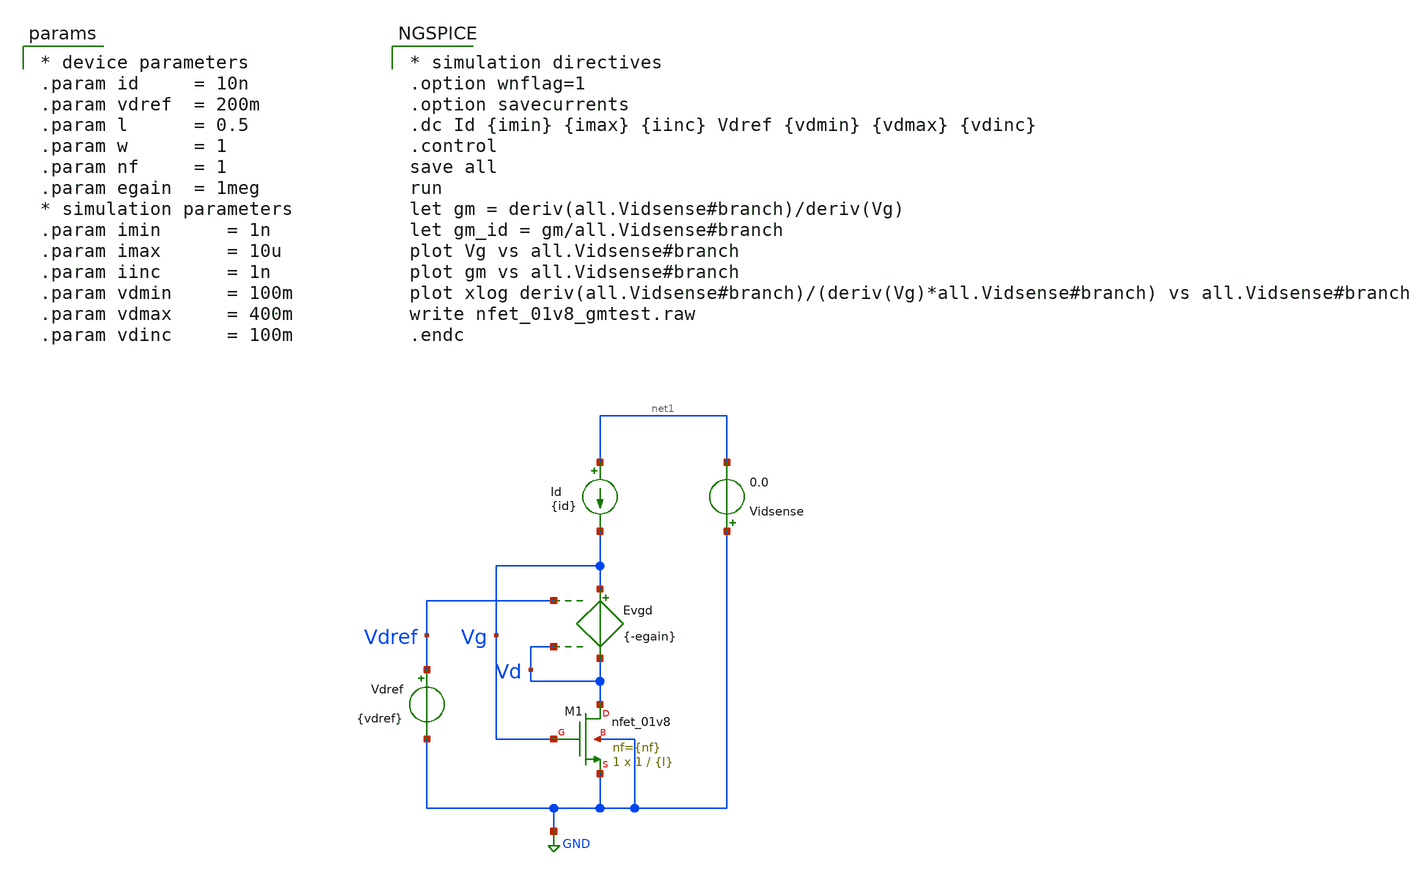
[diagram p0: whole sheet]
** sch_path: xschem/nfet_01v8_gmtest.sch
**.subckt nfet_01v8_gmtest
Evgd Vg Vd Vdref Vd {-egain}
Id net1 Vg {id}
Vdref Vdref GND {vdref}
Vidsense GND net1 0.0
XM1 Vd Vg GND GND sky130_fd_pr__nfet_01v8 L={l} W=1 nf={nf} ad='int((nf+1)/2) * W/nf * 0.29' as='int((nf+2)/2) * W/nf * 0.29'
+ pd='2*int((nf+1)/2) * (W/nf + 0.29)' ps='2*int((nf+2)/2) * (W/nf + 0.29)' nrd='0.29 / W' nrs='0.29 / W'
+ sa=0 sb=0 sd=0 mult=1 m=1
**** begin user architecture code

** opencircuitdesign pdks install
.lib $::SKYWATER_MODELS/sky130.lib.spice tt



* simulation directives
.option wnflag=1
.option savecurrents
.dc Id {imin} {imax} {iinc} Vdref {vdmin} {vdmax} {vdinc}
.control
save all
run
let gm = deriv(all.Vidsense#branch)/deriv(Vg)
let gm_id = gm/all.Vidsense#branch
plot Vg vs all.Vidsense#branch
plot gm vs all.Vidsense#branch
plot xlog deriv(all.Vidsense#branch)/(deriv(Vg)*all.Vidsense#branch) vs all.Vidsense#branch
write nfet_01v8_gmtest.raw
.endc



* device parameters
.param id     = 10n
.param vdref  = 200m
.param l      = 0.5
.param w      = 1
.param nf     = 1
.param egain  = 1meg
* simulation parameters
.param imin      = 1n
.param imax      = 10u
.param iinc      = 1n
.param vdmin     = 100m
.param vdmax     = 400m
.param vdinc     = 100m


**** end user architecture code
**.ends
.GLOBAL GND
.end
